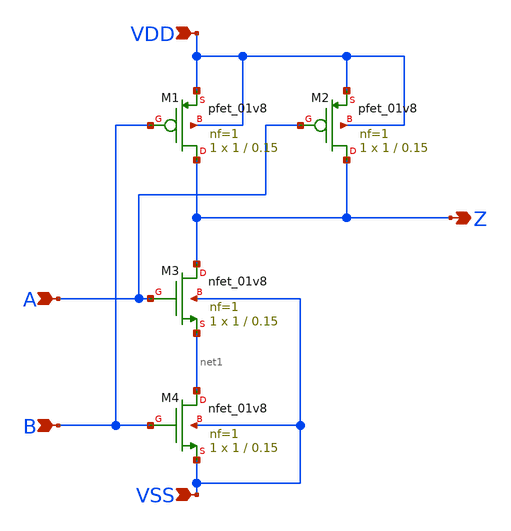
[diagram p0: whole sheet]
** sch_path: NAND.sch
**.subckt NAND A B Z VDD VSS
*.ipin A
*.ipin B
*.opin Z
*.ipin VDD
*.ipin VSS
XM1 Z B VDD VDD sky130_fd_pr__pfet_01v8 L=0.15 W=1 nf=1 ad='int((1 + 1)/2) * 1 / 1 * 0.29' as='int((1 + 2)/2) * 1 / 1 * 0.29'
+ pd='2*int((1 + 1)/2) * (1 / 1 + 0.29)' ps='2*int((1 + 2)/2) * (1 / 1 + 0.29)' nrd='0.29 / 1 ' nrs='0.29 / 1 '
+ sa=0 sb=0 sd=0 mult=1 m=1
XM2 Z A VDD VDD sky130_fd_pr__pfet_01v8 L=0.15 W=1 nf=1 ad='int((1 + 1)/2) * 1 / 1 * 0.29' as='int((1 + 2)/2) * 1 / 1 * 0.29'
+ pd='2*int((1 + 1)/2) * (1 / 1 + 0.29)' ps='2*int((1 + 2)/2) * (1 / 1 + 0.29)' nrd='0.29 / 1 ' nrs='0.29 / 1 '
+ sa=0 sb=0 sd=0 mult=1 m=1
XM3 Z A net1 VSS sky130_fd_pr__nfet_01v8 L=0.15 W=1 nf=1 ad='int((1 + 1)/2) * 1 / 1 * 0.29' as='int((1 + 2)/2) * 1 / 1 * 0.29'
+ pd='2*int((1 + 1)/2) * (1 / 1 + 0.29)' ps='2*int((1 + 2)/2) * (1 / 1 + 0.29)' nrd='0.29 / 1 ' nrs='0.29 / 1 '
+ sa=0 sb=0 sd=0 mult=1 m=1
XM4 net1 B VSS VSS sky130_fd_pr__nfet_01v8 L=0.15 W=1 nf=1 ad='int((1 + 1)/2) * 1 / 1 * 0.29' as='int((1 + 2)/2) * 1 / 1 * 0.29'
+ pd='2*int((1 + 1)/2) * (1 / 1 + 0.29)' ps='2*int((1 + 2)/2) * (1 / 1 + 0.29)' nrd='0.29 / 1 ' nrs='0.29 / 1 '
+ sa=0 sb=0 sd=0 mult=1 m=1
**.ends
.end
